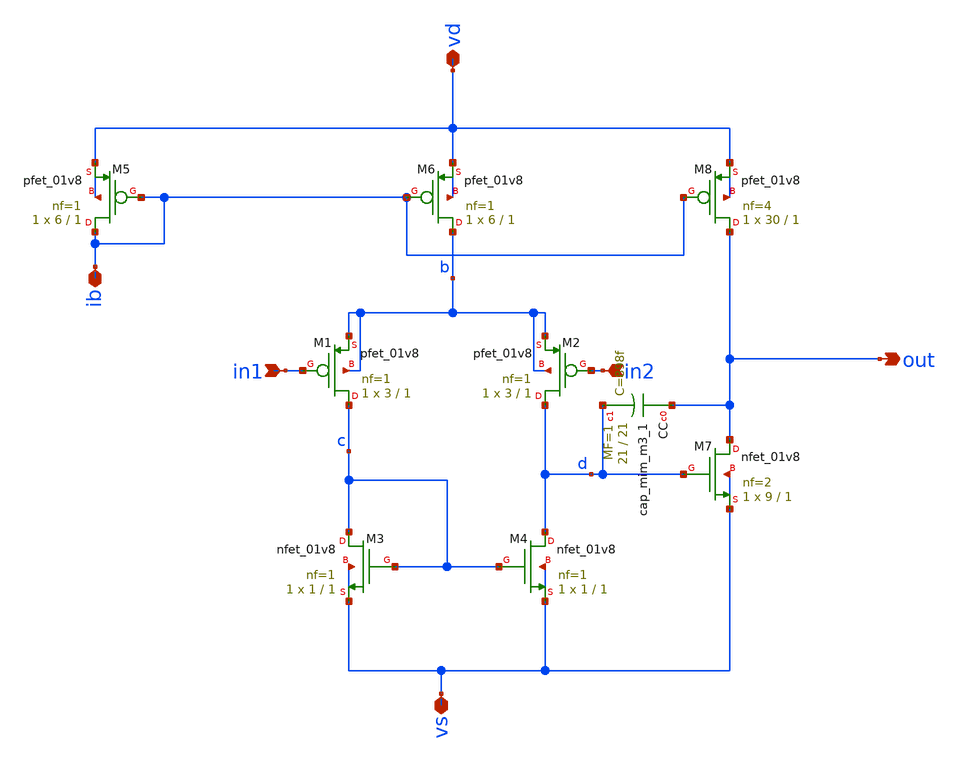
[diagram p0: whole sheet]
** sch_path: amp-op/xschem/ota.sch
* Copyright 2020 Stefan Frederik Schippers
* Licensed under the Apache License, Version 2.0 (the "License");
* you may not use this file except in compliance with the License.
* You may obtain a copy of the License at
* https://www.apache.org/licenses/LICENSE-2.0
* Unless required by applicable law or agreed to in writing, software
* distributed under the License is distributed on an "AS IS" BASIS,
* WITHOUT WARRANTIES OR CONDITIONS OF ANY KIND, either express or implied.
* See the License for the specific language governing permissions and
* limitations under the License.
**.subckt ota vd vs ib in1 in2 out
*.iopin vd
*.iopin vs
*.iopin ib
*.ipin in1
*.ipin in2
*.opin out
XCC out d sky130_fd_pr__cap_mim_m3_1 W=21 L=21 MF=1 m=1
XM5 ib ib vd vd sky130_fd_pr__pfet_01v8 L=1 W=6 nf=1 ad='int((nf+1)/2) * W/nf * 0.29' as='int((nf+2)/2) * W/nf * 0.29'
+ pd='2*int((nf+1)/2) * (W/nf + 0.29)' ps='2*int((nf+2)/2) * (W/nf + 0.29)' nrd='0.29 / W' nrs='0.29 / W'
+ sa=0 sb=0 sd=0 mult=1 m=1
XM6 b ib vd vd sky130_fd_pr__pfet_01v8 L=1 W=6 nf=1 ad='int((nf+1)/2) * W/nf * 0.29' as='int((nf+2)/2) * W/nf * 0.29'
+ pd='2*int((nf+1)/2) * (W/nf + 0.29)' ps='2*int((nf+2)/2) * (W/nf + 0.29)' nrd='0.29 / W' nrs='0.29 / W'
+ sa=0 sb=0 sd=0 mult=1 m=1
XM8 out ib vd vd sky130_fd_pr__pfet_01v8 L=1 W=30 nf=4 ad='int((nf+1)/2) * W/nf * 0.29' as='int((nf+2)/2) * W/nf * 0.29'
+ pd='2*int((nf+1)/2) * (W/nf + 0.29)' ps='2*int((nf+2)/2) * (W/nf + 0.29)' nrd='0.29 / W' nrs='0.29 / W'
+ sa=0 sb=0 sd=0 mult=1 m=1
XM1 c in1 b b sky130_fd_pr__pfet_01v8 L=1 W=3 nf=1 ad='int((nf+1)/2) * W/nf * 0.29' as='int((nf+2)/2) * W/nf * 0.29'
+ pd='2*int((nf+1)/2) * (W/nf + 0.29)' ps='2*int((nf+2)/2) * (W/nf + 0.29)' nrd='0.29 / W' nrs='0.29 / W'
+ sa=0 sb=0 sd=0 mult=1 m=1
XM2 d in2 b b sky130_fd_pr__pfet_01v8 L=1 W=3 nf=1 ad='int((nf+1)/2) * W/nf * 0.29' as='int((nf+2)/2) * W/nf * 0.29'
+ pd='2*int((nf+1)/2) * (W/nf + 0.29)' ps='2*int((nf+2)/2) * (W/nf + 0.29)' nrd='0.29 / W' nrs='0.29 / W'
+ sa=0 sb=0 sd=0 mult=1 m=1
XM3 c c vs vs sky130_fd_pr__nfet_01v8 L=1 W=1 nf=1 ad='int((nf+1)/2) * W/nf * 0.29' as='int((nf+2)/2) * W/nf * 0.29'
+ pd='2*int((nf+1)/2) * (W/nf + 0.29)' ps='2*int((nf+2)/2) * (W/nf + 0.29)' nrd='0.29 / W' nrs='0.29 / W'
+ sa=0 sb=0 sd=0 mult=1 m=1
XM4 d c vs vs sky130_fd_pr__nfet_01v8 L=1 W=1 nf=1 ad='int((nf+1)/2) * W/nf * 0.29' as='int((nf+2)/2) * W/nf * 0.29'
+ pd='2*int((nf+1)/2) * (W/nf + 0.29)' ps='2*int((nf+2)/2) * (W/nf + 0.29)' nrd='0.29 / W' nrs='0.29 / W'
+ sa=0 sb=0 sd=0 mult=1 m=1
XM7 out d vs vs sky130_fd_pr__nfet_01v8 L=1 W=9 nf=2 ad='int((nf+1)/2) * W/nf * 0.29' as='int((nf+2)/2) * W/nf * 0.29'
+ pd='2*int((nf+1)/2) * (W/nf + 0.29)' ps='2*int((nf+2)/2) * (W/nf + 0.29)' nrd='0.29 / W' nrs='0.29 / W'
+ sa=0 sb=0 sd=0 mult=1 m=1
**.ends
.end
